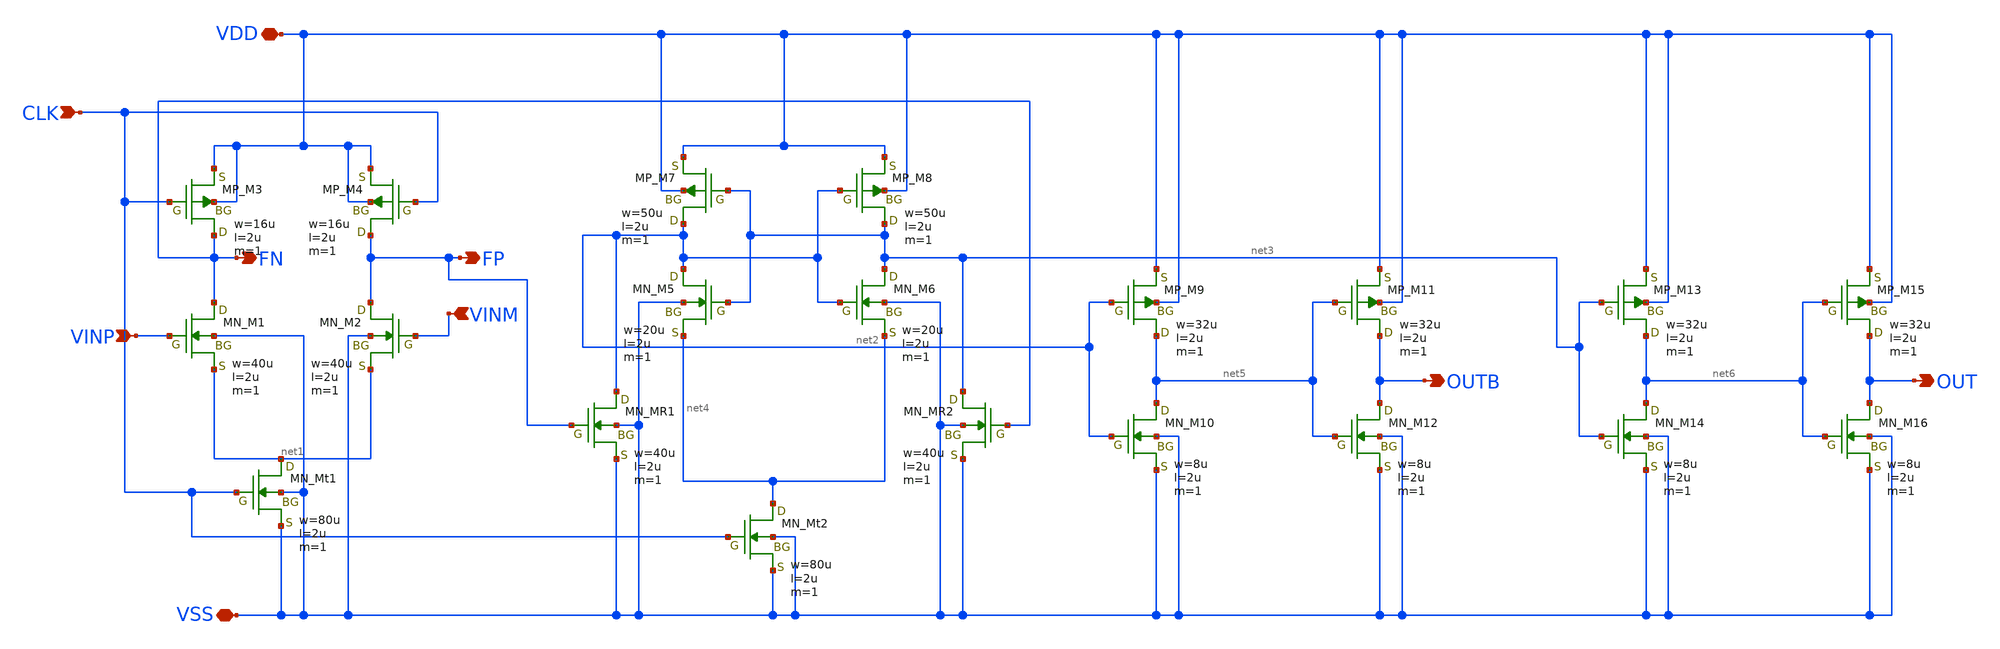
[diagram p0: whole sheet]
** sch_path: member_project/opamp/zawa/comp3.sch
**.subckt comp3 VSS VDD CLK VINP VINM FN FP OUTB OUT
*.iopin VSS
*.iopin VDD
*.ipin CLK
*.ipin VINP
*.ipin VINM
*.opin FN
*.opin FP
*.opin OUTB
*.opin OUT
M3 FN CLK VDD VDD PMOS w=16u l=2u as=0 ad=0 ps=0 pd=0 nrd=0 nrs=0 m=1
M1 FN VINP net1 VSS NMOS w=40u l=2u as=0 ad=0 ps=0 pd=0 nrd=0 nrs=0 m=1
Mt1 net1 CLK VSS VSS NMOS w=80u l=2u as=0 ad=0 ps=0 pd=0 nrd=0 nrs=0 m=1
M7 net2 net3 VDD VDD PMOS w=50u l=2u as=0 ad=0 ps=0 pd=0 nrd=0 nrs=0 m=1
M5 net2 net3 net4 VSS NMOS w=20u l=2u as=0 ad=0 ps=0 pd=0 nrd=0 nrs=0 m=1
MR1 net2 FP VSS VSS NMOS w=40u l=2u as=0 ad=0 ps=0 pd=0 nrd=0 nrs=0 m=1
Mt2 net4 CLK VSS VSS NMOS w=80u l=2u as=0 ad=0 ps=0 pd=0 nrd=0 nrs=0 m=1
M2 FP VINM net1 VSS NMOS w=40u l=2u as=0 ad=0 ps=0 pd=0 nrd=0 nrs=0 m=1
M4 FP CLK VDD VDD PMOS w=16u l=2u as=0 ad=0 ps=0 pd=0 nrd=0 nrs=0 m=1
MR2 net3 FN VSS VSS NMOS w=40u l=2u as=0 ad=0 ps=0 pd=0 nrd=0 nrs=0 m=1
M6 net3 net2 net4 VSS NMOS w=20u l=2u as=0 ad=0 ps=0 pd=0 nrd=0 nrs=0 m=1
M8 net3 net2 VDD VDD PMOS w=50u l=2u as=0 ad=0 ps=0 pd=0 nrd=0 nrs=0 m=1
M9 net5 net2 VDD VDD PMOS w=32u l=2u as=0 ad=0 ps=0 pd=0 nrd=0 nrs=0 m=1
M10 net5 net2 VSS VSS NMOS w=8u l=2u as=0 ad=0 ps=0 pd=0 nrd=0 nrs=0 m=1
M11 OUTB net5 VDD VDD PMOS w=32u l=2u as=0 ad=0 ps=0 pd=0 nrd=0 nrs=0 m=1
M12 OUTB net5 VSS VSS NMOS w=8u l=2u as=0 ad=0 ps=0 pd=0 nrd=0 nrs=0 m=1
M13 net6 net3 VDD VDD PMOS w=32u l=2u as=0 ad=0 ps=0 pd=0 nrd=0 nrs=0 m=1
M14 net6 net3 VSS VSS NMOS w=8u l=2u as=0 ad=0 ps=0 pd=0 nrd=0 nrs=0 m=1
M15 OUT net6 VDD VDD PMOS w=32u l=2u as=0 ad=0 ps=0 pd=0 nrd=0 nrs=0 m=1
M16 OUT net6 VSS VSS NMOS w=8u l=2u as=0 ad=0 ps=0 pd=0 nrd=0 nrs=0 m=1
**** begin user architecture code
 .include $::LIB/ip62_models

VSS_SRC VSS 0 DC 0
VDD_SRC VDD VSS DC 5

* CLK: 周期20ns、最初の20nsはリセット
VCLK CLK VSS PULSE(0 5 20n 3n 3n 15n 26n)

* 差動で振ってコモンモードを2.5Vに固定
*VINP_SRC VINP VSS PWL(0 2.480 1000n 2.520)
*VINM_SRC VINM VSS PWL(0 2.520 1000n 2.480)
VINM_SRC VINM VSS DC 2.5
VINP_SRC VINP VSS PWL(0 0 1000n 5)
* 次段バッファ相当の負荷
*CL1 OUT  VSS 100f
*CL2 OUTB VSS 100f

.options reltol=1e-4 abstol=1e-13 vntol=1e-7

.control
save all

tran 0.02n 1000n

* リセット期間の静的電流（ゼロなら正常）
meas tran i_static AVG i(vdd_src) from=15n to=19n

plot v(CLK)
plot v(VINP) v(VINM)
plot v(FN) v(FP)
plot v(OUT) v(OUTB)
plot i(vdd_src)
plot v(OUT)
plot v(OUTB)
.endc

**** end user architecture code
**.ends
.end
